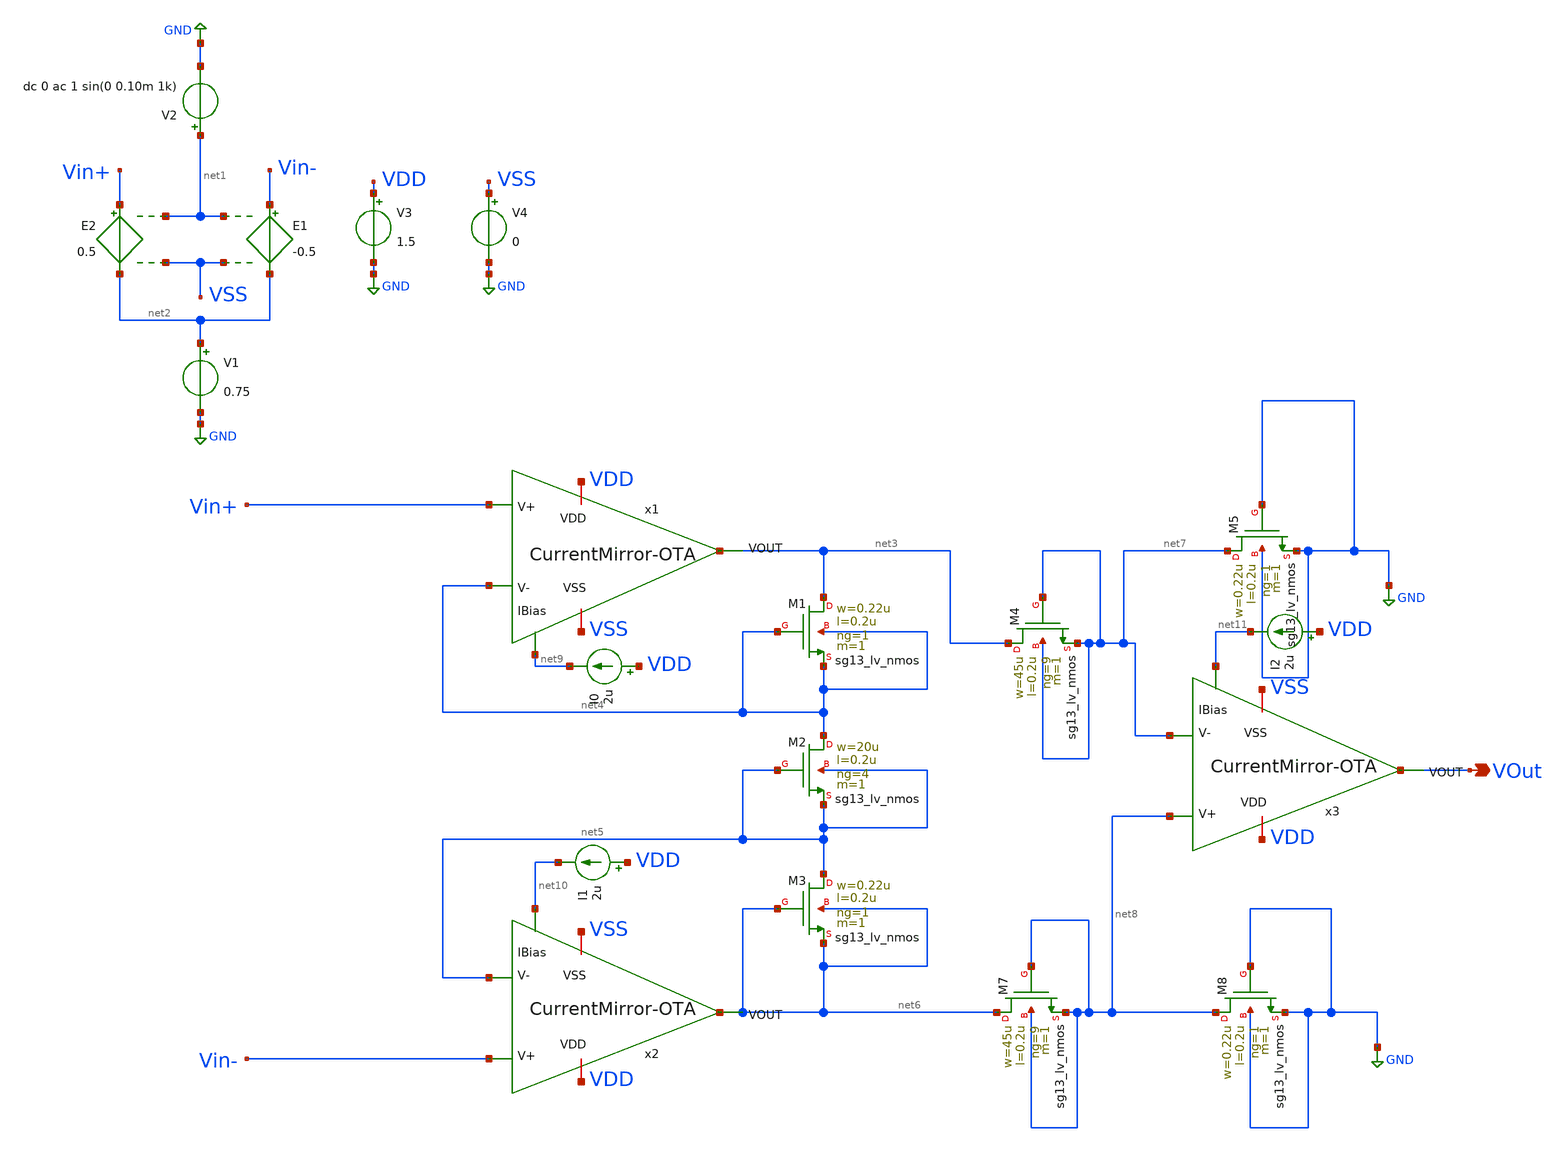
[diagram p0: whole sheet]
** sch_path: INA/testbench_ina.sch
**.subckt testbench_ina VOut
*.opin VOut
x1 VDD Vin+ net4 net9 net3 VSS CurrentMirror-OTA
x2 VDD Vin- net5 net10 net6 VSS CurrentMirror-OTA
x3 VDD net8 net7 net11 VOut VSS CurrentMirror-OTA
E1 Vin- net2 net1 VSS -0.5
E2 Vin+ net2 net1 VSS 0.5
V1 net2 GND 0.75
V2 net1 GND dc 0 ac 1 sin(0 0.10m 1k)
V3 VDD GND 1.5
V4 VSS GND 0
XM1 net3 net4 net4 net4 sg13_lv_nmos w=0.22u l=0.2u ng=1 m=1 mm_ok=1
XM2 net4 net5 net5 net5 sg13_lv_nmos w=20u l=0.2u ng=4 m=1 mm_ok=1
XM3 net5 net6 net6 net6 sg13_lv_nmos w=0.22u l=0.2u ng=1 m=1 mm_ok=1
XM4 net3 net7 net7 net7 sg13_lv_nmos w=45u l=0.2u ng=9 m=1 mm_ok=1
XM5 net7 GND GND GND sg13_lv_nmos w=0.22u l=0.2u ng=1 m=1 mm_ok=1
XM7 net6 net8 net8 net8 sg13_lv_nmos w=45u l=0.2u ng=9 m=1 mm_ok=1
XM8 net8 GND GND GND sg13_lv_nmos w=0.22u l=0.2u ng=1 m=1 mm_ok=1
I0 VDD net9 2u
I1 VDD net10 2u
I2 VDD net11 2u
**** begin user architecture code

.lib cornerMOSlv.lib mos_tt
.lib cornerMOShv.lib mos_tt
.lib $::SG13G2_MODELS/cornerCAP.lib cap_typ



.param temp=27
.save all

.save @n.xm1.nsg13_lv_nmos[gds]
.save @n.xm2.nsg13_lv_nmos[gds]
.save @n.xm3.nsg13_lv_nmos[gds]
.save @n.xm4.nsg13_lv_nmos[gds]
.save @n.xm5.nsg13_lv_nmos[gds]
.save @n.xm7.nsg13_lv_nmos[gds]
.save @n.xm8.nsg13_lv_nmos[gds]



.control
   ac dec 20 0.1 21meg
   set filetype = ascii
   set units=degrees
   write testbench_ina.raw vdb(vout) vp(vout)
   set appendwrite
   op
   set filetype = ascii
   write testbench_ina.raw

  * tran 0.1u 2111u
  * set filetype = ascii
  * write testbench_ina.raw v(vin+) v(vin-) v(vout)
  * set appendwrite
  * op
  * set filetype = ascii
  * write testbench_ina.raw

.endc


**** end user architecture code
**.ends

* expanding   symbol:  /home/designer/shared/Design/CCLNA/CurrentMirror-OTA.sym # of pins=6
** sym_path: BPF/CurrentMirror-OTA.sym
** sch_path: BPF/CurrentMirror-OTA.sch
.subckt CurrentMirror-OTA VDD V+ V- IBias VOUT VSS
*.iopin VDD
*.iopin VSS
*.ipin V-
*.opin VOUT
*.ipin V+
*.ipin IBias
XM4 net1 net1 VDD VDD sg13_lv_pmos w=4u l=1u ng=1 m=1 mm_ok=1
XM3 net4 net1 VDD VDD sg13_lv_pmos w=4u l=1u ng=1 m=3 mm_ok=1
XM5 net2 net2 VDD VDD sg13_lv_pmos w=4u l=1u ng=1 m=1 mm_ok=1
XM6 VOUT net2 VDD VDD sg13_lv_pmos w=4u l=1u ng=1 m=3 mm_ok=1
XM7 net1 V- net3 net3 sg13_lv_nmos w=8u l=1u ng=1 m=1 mm_ok=1
XM8 net2 V+ net3 net3 sg13_lv_nmos w=8u l=1u ng=1 m=1 mm_ok=1
XM9 net3 IBias VSS VSS sg13_lv_nmos w=2u l=1u ng=1 m=1 mm_ok=1
XM10 IBias IBias VSS VSS sg13_lv_nmos w=2u l=1u ng=1 m=1 mm_ok=1
XM11 net4 net4 VSS VSS sg13_lv_nmos w=3u l=1u ng=1 m=1 mm_ok=1
XM12 VOUT net4 VSS VSS sg13_lv_nmos w=3u l=1u ng=1 m=1 mm_ok=1
.ends

.GLOBAL GND
.end
